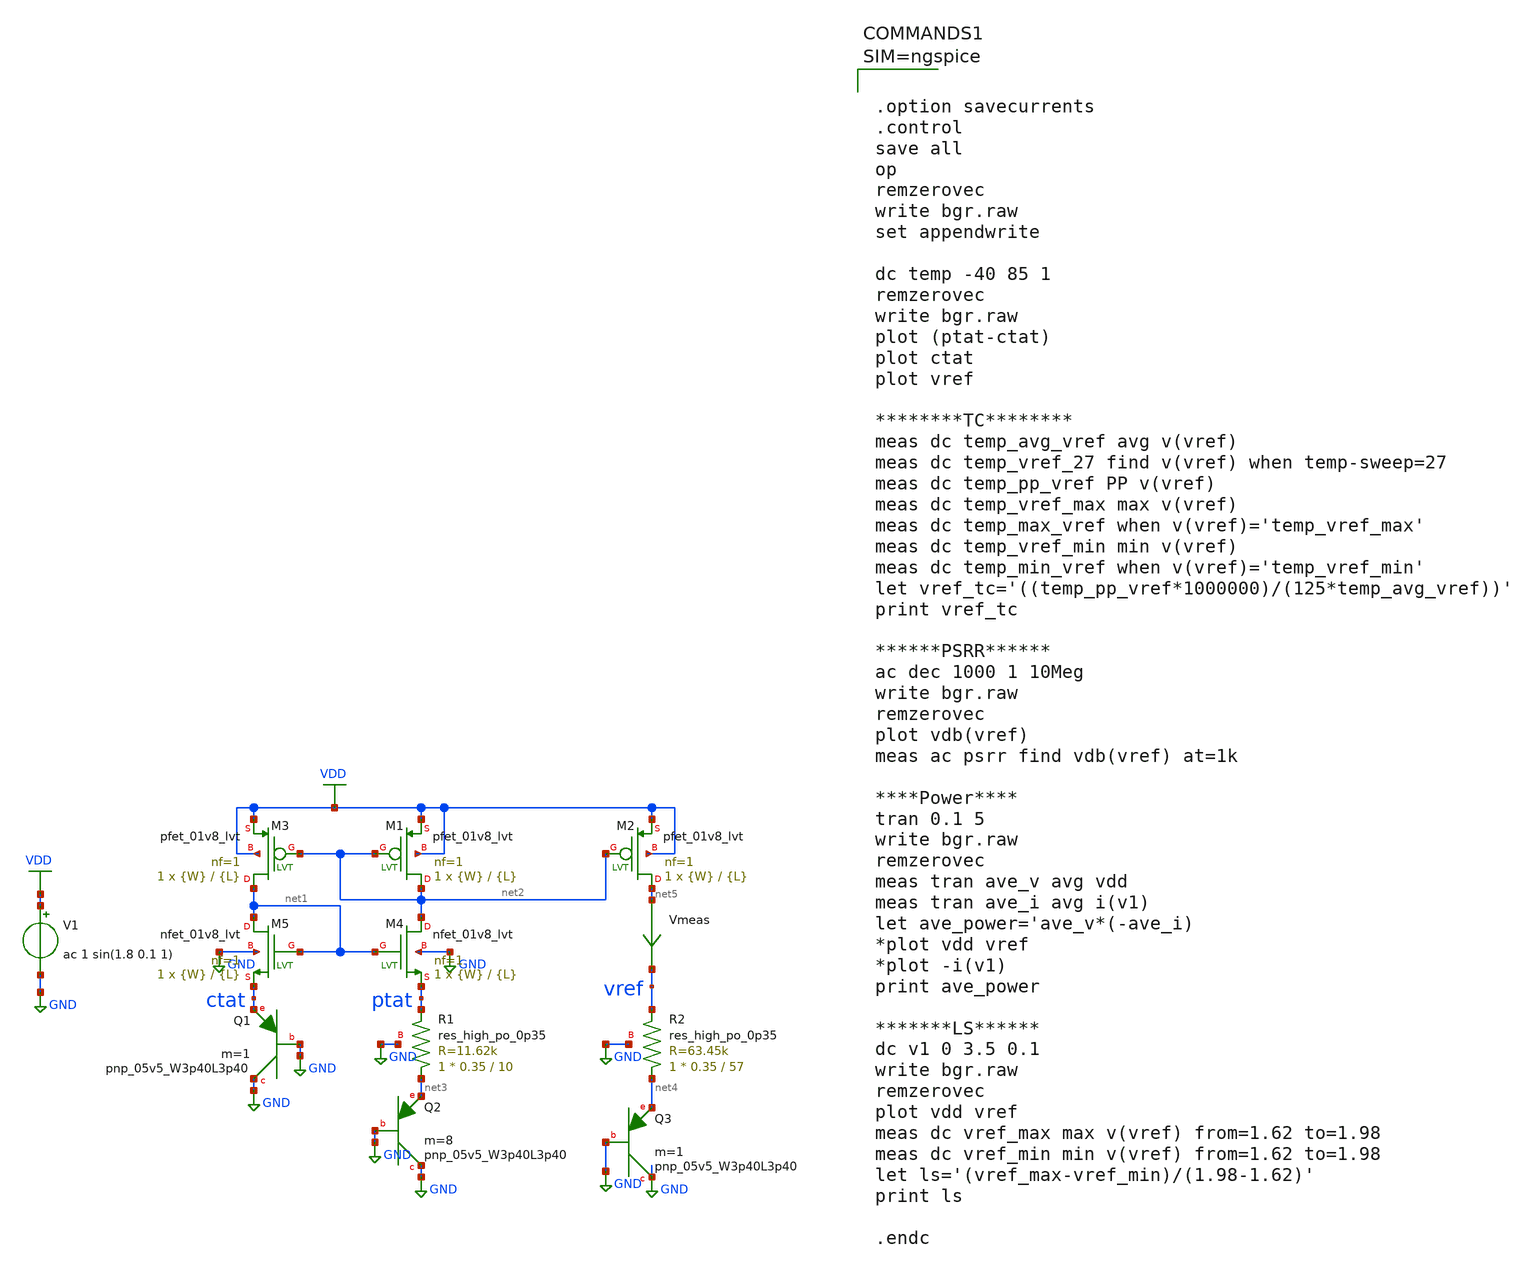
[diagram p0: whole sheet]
** sch_path: xschem/bgr.sch
**.subckt bgr
V1 VDD GND ac 1 sin(1.8 0.1 1)
XQ1 GND GND ctat sky130_fd_pr__pnp_05v5_W3p40L3p40 m=1
XQ2 GND GND net3 sky130_fd_pr__pnp_05v5_W3p40L3p40 m=8
XQ3 GND GND net4 sky130_fd_pr__pnp_05v5_W3p40L3p40 m=1
Vmeas net5 vref 0
.save i(vmeas)
XM3 net1 net2 VDD VDD sky130_fd_pr__pfet_01v8_lvt L={L} W={W} nf=1 ad='int((nf+1)/2) * W/nf * 0.29' as='int((nf+2)/2) * W/nf * 0.29'
+ pd='2*int((nf+1)/2) * (W/nf + 0.29)' ps='2*int((nf+2)/2) * (W/nf + 0.29)' nrd='0.29 / W' nrs='0.29 / W'
+ sa=0 sb=0 sd=0 mult=1 m=1
XM1 net2 net2 VDD VDD sky130_fd_pr__pfet_01v8_lvt L={L} W={W} nf=1 ad='int((nf+1)/2) * W/nf * 0.29' as='int((nf+2)/2) * W/nf * 0.29'
+ pd='2*int((nf+1)/2) * (W/nf + 0.29)' ps='2*int((nf+2)/2) * (W/nf + 0.29)' nrd='0.29 / W' nrs='0.29 / W'
+ sa=0 sb=0 sd=0 mult=1 m=1
XM2 net5 net2 VDD VDD sky130_fd_pr__pfet_01v8_lvt L={L} W={W} nf=1 ad='int((nf+1)/2) * W/nf * 0.29' as='int((nf+2)/2) * W/nf * 0.29'
+ pd='2*int((nf+1)/2) * (W/nf + 0.29)' ps='2*int((nf+2)/2) * (W/nf + 0.29)' nrd='0.29 / W' nrs='0.29 / W'
+ sa=0 sb=0 sd=0 mult=1 m=1
XM5 net1 net1 ctat GND sky130_fd_pr__nfet_01v8_lvt L={L} W={W} nf=1 ad='int((nf+1)/2) * W/nf * 0.29'
+ as='int((nf+2)/2) * W/nf * 0.29' pd='2*int((nf+1)/2) * (W/nf + 0.29)' ps='2*int((nf+2)/2) * (W/nf + 0.29)'
+ nrd='0.29 / W' nrs='0.29 / W' sa=0 sb=0 sd=0 mult=1 m=1
XM4 net2 net1 ptat GND sky130_fd_pr__nfet_01v8_lvt L={L} W={W} nf=1 ad='int((nf+1)/2) * W/nf * 0.29'
+ as='int((nf+2)/2) * W/nf * 0.29' pd='2*int((nf+1)/2) * (W/nf + 0.29)' ps='2*int((nf+2)/2) * (W/nf + 0.29)'
+ nrd='0.29 / W' nrs='0.29 / W' sa=0 sb=0 sd=0 mult=1 m=1
XR1 net3 ptat GND sky130_fd_pr__res_high_po_0p35 L=10 mult=1 m=1
XR2 net4 vref GND sky130_fd_pr__res_high_po_0p35 L=57 mult=1 m=1
**** begin user architecture code

** opencircuitdesign pdks install
.lib $::SKYWATER_MODELS/sky130.lib.spice tt




.param L=1.5
.param W=80





.option savecurrents
.control
save all
op
remzerovec
write bgr.raw
set appendwrite

dc temp -40 85 1
remzerovec
write bgr.raw
plot (ptat-ctat)
plot ctat
plot vref

********TC********
meas dc temp_avg_vref avg v(vref)
meas dc temp_vref_27 find v(vref) when temp-sweep=27
meas dc temp_pp_vref PP v(vref)
meas dc temp_vref_max max v(vref)
meas dc temp_max_vref when v(vref)='temp_vref_max'
meas dc temp_vref_min min v(vref)
meas dc temp_min_vref when v(vref)='temp_vref_min'
let vref_tc='((temp_pp_vref*1000000)/(125*temp_avg_vref))'
print vref_tc

******PSRR******
ac dec 1000 1 10Meg
write bgr.raw
remzerovec
plot vdb(vref)
meas ac psrr find vdb(vref) at=1k

****Power****
tran 0.1 5
write bgr.raw
remzerovec
meas tran ave_v avg vdd
meas tran ave_i avg i(v1)
let ave_power='ave_v*(-ave_i)
*plot vdd vref
*plot -i(v1)
print ave_power

*******LS******
dc v1 0 3.5 0.1
write bgr.raw
remzerovec
plot vdd vref
meas dc vref_max max v(vref) from=1.62 to=1.98
meas dc vref_min min v(vref) from=1.62 to=1.98
let ls='(vref_max-vref_min)/(1.98-1.62)'
print ls

.endc



**** end user architecture code
**.ends
.GLOBAL VDD
.GLOBAL GND
.end
